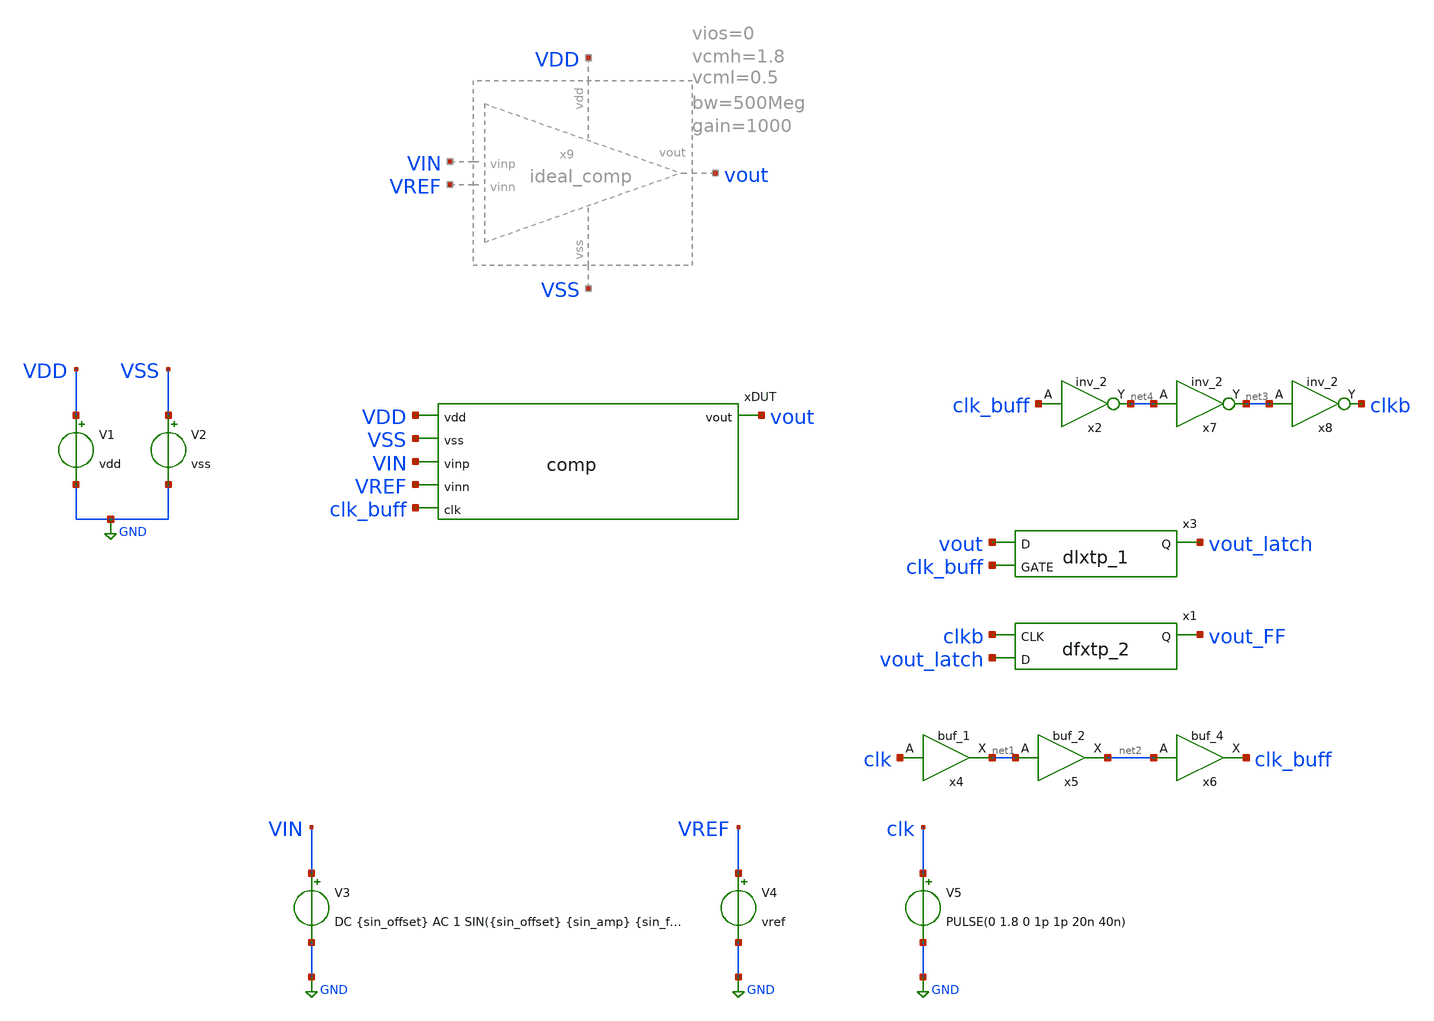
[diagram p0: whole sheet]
** sch_path: simulation/tb_comp.sch
**.subckt tb_comp
V1 VDD GND vdd
V2 VSS GND vss
V3 VIN GND DC {sin_offset} AC 1 SIN({sin_offset} {sin_amp} {sin_freq})
V4 VREF GND vref
xDUT vout VDD VSS VIN VREF clk_buff comp
V5 clk GND PULSE(0 1.8 0 1p 1p 20n 40n)
x2 clk_buff vss vss vdd vdd net4 sky130_fd_sc_hd__inv_2
x3 vout clk_buff vss vss vdd vdd vout_latch sky130_fd_sc_hd__dlxtp_1
x1 clkb vout_latch vss vss vdd vdd vout_FF sky130_fd_sc_hd__dfxtp_2
x4 clk vss vss vdd vdd net1 sky130_fd_sc_hd__buf_1
x5 net1 vss vss vdd vdd net2 sky130_fd_sc_hd__buf_2
x6 net2 vss vss vdd vdd clk_buff sky130_fd_sc_hd__buf_4
x7 net4 vss vss vdd vdd net3 sky130_fd_sc_hd__inv_2
x8 net3 vss vss vdd vdd clkb sky130_fd_sc_hd__inv_2
**** begin user architecture code



# Model files
.lib /usr/local/share/pdk/sky130A/libs.tech/ngspice/sky130.lib.spice tt
.include /usr/local/share/pdk/sky130A/libs.ref/sky130_fd_sc_hd/spice/sky130_fd_sc_hd.spice

.options method=gear reltol=1e-6 abstol=1e-12

# Main parameters
.param vdd=1.8 vss=0 vref='900m' vhigh=1.8 vlow=0
.param sin_offset='vdd/2'
.param sin_amp='vdd/2'
.param sin_freq=10e6
.param sin_period='1/sin_freq'
.param tran_step='25e-12'
.param tran_stop_time='sin_period*3'

# Component parameters



# Save settings
.save


# Analysis
.op
.dc V3 0 {vdd} {vdd/20}
.tran {tran_step} {tran_stop_time}
.ac dec 50 1e3 1e10

# Start control block
.control


# Run sim
run
write tb_comp.raw

#set appendwrite
#alterparam vref='100m'
#reset
#run
#write tb_comp.raw

#alterparam vref='1.7'
#reset
#run
#write tb_comp.raw



.endc



**** end user architecture code
**.ends

* expanding   symbol:  schematics/comp.sym # of pins=6
** sym_path: schematics/comp.sym
** sch_path: schematics/comp.sch
.subckt comp vout vdd vss vinp vinn clk
*.ipin vdd
*.opin vout
*.ipin vss
*.ipin vinp
*.ipin vinn
*.ipin clk
XM6 net1 clk vss vss sky130_fd_pr__nfet_01v8 L=0.15 W=1 nf=1 ad='int((1 + 1)/2) * 1 / 1 * 0.29' as='int((1 + 2)/2) * 1 / 1 * 0.29'
+ pd='2*int((1 + 1)/2) * (1 / 1 + 0.29)' ps='2*int((1 + 2)/2) * (1 / 1 + 0.29)' nrd='0.29 / 1 ' nrs='0.29 / 1 '
+ sa=0 sb=0 sd=0 mult=1 m=1
XM10 voutn voutp vdd vdd sky130_fd_pr__pfet_01v8 L=0.15 W=1 nf=1 ad='int((1 + 1)/2) * 1 / 1 * 0.29' as='int((1 + 2)/2) * 1 / 1 * 0.29'
+ pd='2*int((1 + 1)/2) * (1 / 1 + 0.29)' ps='2*int((1 + 2)/2) * (1 / 1 + 0.29)' nrd='0.29 / 1 ' nrs='0.29 / 1 '
+ sa=0 sb=0 sd=0 mult=1 m=1
xBUFF voutp vss vss vdd vdd voutp_buff sky130_fd_sc_hd__buf_6
xBUFF1 voutn vss vss vdd vdd voutn_buff sky130_fd_sc_hd__buf_6
I0 pa_m1_s vss 10u
XM11 v_m1_d voutp_buff pa_m1_s vss sky130_fd_pr__nfet_01v8 L=0.15 W=50 nf=1 ad='int((1 + 1)/2) * 50 / 1 * 0.29'
+ as='int((1 + 2)/2) * 50 / 1 * 0.29' pd='2*int((1 + 1)/2) * (50 / 1 + 0.29)' ps='2*int((1 + 2)/2) * (50 / 1 + 0.29)'
+ nrd='0.29 / 50 ' nrs='0.29 / 50 ' sa=0 sb=0 sd=0 mult=1 m=1
XM12 vout voutn_buff pa_m1_s vss sky130_fd_pr__nfet_01v8 L=0.15 W=50 nf=1 ad='int((1 + 1)/2) * 50 / 1 * 0.29'
+ as='int((1 + 2)/2) * 50 / 1 * 0.29' pd='2*int((1 + 1)/2) * (50 / 1 + 0.29)' ps='2*int((1 + 2)/2) * (50 / 1 + 0.29)'
+ nrd='0.29 / 50 ' nrs='0.29 / 50 ' sa=0 sb=0 sd=0 mult=1 m=1
XM13 v_m1_d v_m1_d vdd vdd sky130_fd_pr__pfet_01v8 L=0.5 W=2 nf=1 ad='int((1 + 1)/2) * 2 / 1 * 0.29'
+ as='int((1 + 2)/2) * 2 / 1 * 0.29' pd='2*int((1 + 1)/2) * (2 / 1 + 0.29)' ps='2*int((1 + 2)/2) * (2 / 1 + 0.29)'
+ nrd='0.29 / 2 ' nrs='0.29 / 2 ' sa=0 sb=0 sd=0 mult=1 m=1
XM14 vout v_m1_d vdd vdd sky130_fd_pr__pfet_01v8 L=0.5 W=2 nf=1 ad='int((1 + 1)/2) * 2 / 1 * 0.29' as='int((1 + 2)/2) * 2 / 1 * 0.29'
+ pd='2*int((1 + 1)/2) * (2 / 1 + 0.29)' ps='2*int((1 + 2)/2) * (2 / 1 + 0.29)' nrd='0.29 / 2 ' nrs='0.29 / 2 '
+ sa=0 sb=0 sd=0 mult=1 m=1
XM1 vinp_d vinp net1 vss sky130_fd_pr__nfet_01v8 L=0.15 W=20 nf=1 ad='int((1 + 1)/2) * 20 / 1 * 0.29'
+ as='int((1 + 2)/2) * 20 / 1 * 0.29' pd='2*int((1 + 1)/2) * (20 / 1 + 0.29)' ps='2*int((1 + 2)/2) * (20 / 1 + 0.29)'
+ nrd='0.29 / 20 ' nrs='0.29 / 20 ' sa=0 sb=0 sd=0 mult=1 m=1
XM2 vinn_d vinn net1 vss sky130_fd_pr__nfet_01v8 L=0.15 W=20 nf=1 ad='int((1 + 1)/2) * 20 / 1 * 0.29'
+ as='int((1 + 2)/2) * 20 / 1 * 0.29' pd='2*int((1 + 1)/2) * (20 / 1 + 0.29)' ps='2*int((1 + 2)/2) * (20 / 1 + 0.29)'
+ nrd='0.29 / 20 ' nrs='0.29 / 20 ' sa=0 sb=0 sd=0 mult=1 m=1
XM3 voutn voutp vinp_d vss sky130_fd_pr__nfet_01v8 L=0.15 W=1 nf=1 ad='int((1 + 1)/2) * 1 / 1 * 0.29'
+ as='int((1 + 2)/2) * 1 / 1 * 0.29' pd='2*int((1 + 1)/2) * (1 / 1 + 0.29)' ps='2*int((1 + 2)/2) * (1 / 1 + 0.29)'
+ nrd='0.29 / 1 ' nrs='0.29 / 1 ' sa=0 sb=0 sd=0 mult=1 m=1
XM4 voutp voutn vinn_d vss sky130_fd_pr__nfet_01v8 L=0.15 W=1 nf=1 ad='int((1 + 1)/2) * 1 / 1 * 0.29'
+ as='int((1 + 2)/2) * 1 / 1 * 0.29' pd='2*int((1 + 1)/2) * (1 / 1 + 0.29)' ps='2*int((1 + 2)/2) * (1 / 1 + 0.29)'
+ nrd='0.29 / 1 ' nrs='0.29 / 1 ' sa=0 sb=0 sd=0 mult=1 m=1
XM5 voutp voutn vdd vdd sky130_fd_pr__pfet_01v8 L=0.15 W=1 nf=1 ad='int((1 + 1)/2) * 1 / 1 * 0.29' as='int((1 + 2)/2) * 1 / 1 * 0.29'
+ pd='2*int((1 + 1)/2) * (1 / 1 + 0.29)' ps='2*int((1 + 2)/2) * (1 / 1 + 0.29)' nrd='0.29 / 1 ' nrs='0.29 / 1 '
+ sa=0 sb=0 sd=0 mult=1 m=1
XM7 voutp clk vdd vdd sky130_fd_pr__pfet_01v8 L=0.15 W=1 nf=1 ad='int((1 + 1)/2) * 1 / 1 * 0.29' as='int((1 + 2)/2) * 1 / 1 * 0.29'
+ pd='2*int((1 + 1)/2) * (1 / 1 + 0.29)' ps='2*int((1 + 2)/2) * (1 / 1 + 0.29)' nrd='0.29 / 1 ' nrs='0.29 / 1 '
+ sa=0 sb=0 sd=0 mult=1 m=1
XM8 voutn clk vdd vdd sky130_fd_pr__pfet_01v8 L=0.15 W=1 nf=1 ad='int((1 + 1)/2) * 1 / 1 * 0.29' as='int((1 + 2)/2) * 1 / 1 * 0.29'
+ pd='2*int((1 + 1)/2) * (1 / 1 + 0.29)' ps='2*int((1 + 2)/2) * (1 / 1 + 0.29)' nrd='0.29 / 1 ' nrs='0.29 / 1 '
+ sa=0 sb=0 sd=0 mult=1 m=1
.ends


* expanding   symbol:  schematics/ideal_comp.sym # of pins=5
** sym_path: schematics/ideal_comp.sym
** sch_path: schematics/ideal_comp.sch
.subckt ideal_comp vdd vss vinp vout vinn  bw=100Meg gain=1000 vcmh=1.8 vcml=0 vios=50m
*.ipin vdd
*.opin vout
*.ipin vss
*.ipin vinp
*.ipin vinn
B1 vp vss V = {V(vinp)<vcmh ? (V(vinp) < vcml ? vcml: V(vinp)) : vcmh}
B2 vn vss V = {V(vinn)<vcmh ? (V(vinn) < vcml ? vcml: V(vinn) + vios) : vcmh}
B3 net1 vss V = {gain*(V(vp)-V(vn)) < V(vdd) ? (gain*(V(vp)-V(vn)) < V(vss) ? V(vss) : (gain*(V(vp)-V(vn)))) : V(vdd)}
R1 vout net1 {1/(2*3.1415*bw*1p)} m=1
C1 vout vss 1p m=1
.ends

.GLOBAL GND
.end
